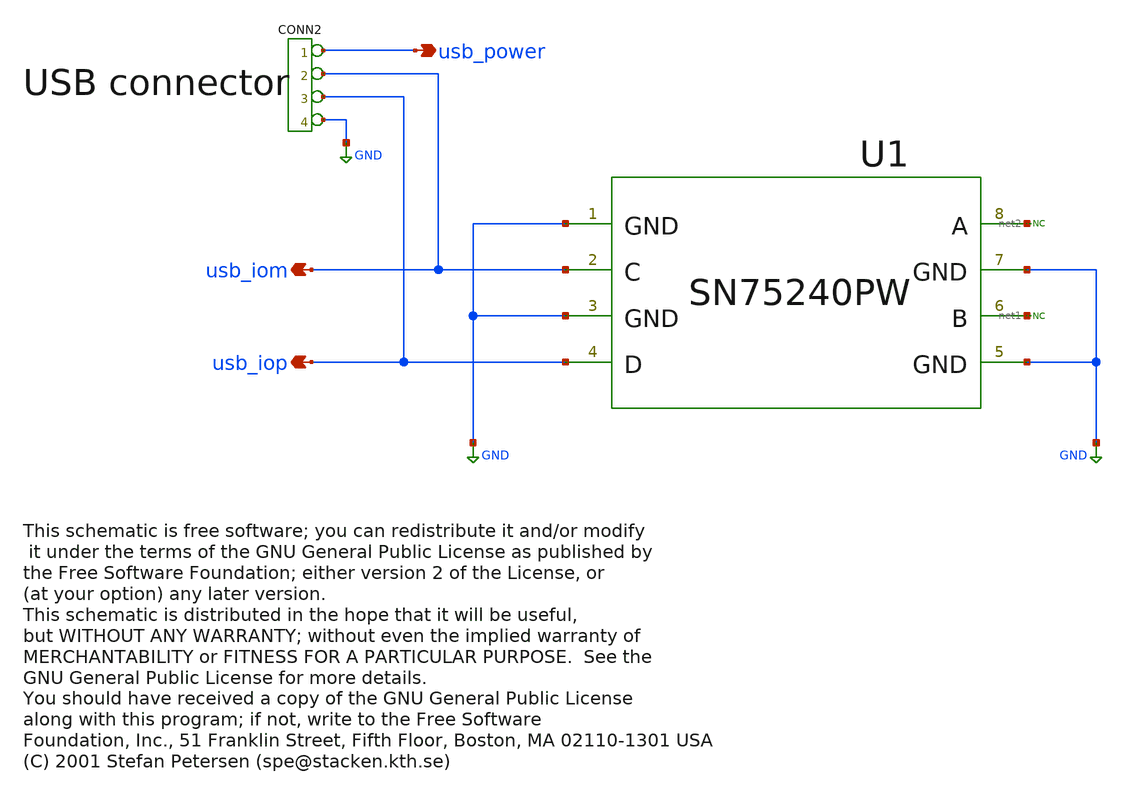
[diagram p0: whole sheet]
** sch_path: xschem_library_oa/xTAG/xTAG-consio/schematic/xTAG-consio.sch
* Copyright (C) 1998-2024 Stefan Frederik Schippers
* This program is free software; you can redistribute it and/or modify
* it under the terms of the GNU General Public License as published by
* the Free Software Foundation; either version 2 of the License, or
* (at your option) any later version.
* This program is distributed in the hope that it will be useful,
* but WITHOUT ANY WARRANTY; without even the implied warranty of
* MERCHANTABILITY or FITNESS FOR A PARTICULAR PURPOSE.  See the
* GNU General Public License for more details.
* You should have received a copy of the GNU General Public License
* along with this program; if not, write to the Free Software
* This schematic is free software; you can redistribute it and/or modify
* (C) 2001 Stefan Petersen (spe@stacken.kth.se)
**.subckt xTAG-consio usb_power usb_iom usb_iop
*.opin usb_power
*.opin usb_iom
*.opin usb_iop
*connector(3,1) ?1 usb_power ?1 usb_iom ?1 usb_iop ?1 GND
U1 GND usb_iom usb_iop net1 net2 sn75240pw
* noconn #net1
* noconn #net2
**.ends
.GLOBAL GND
.end
